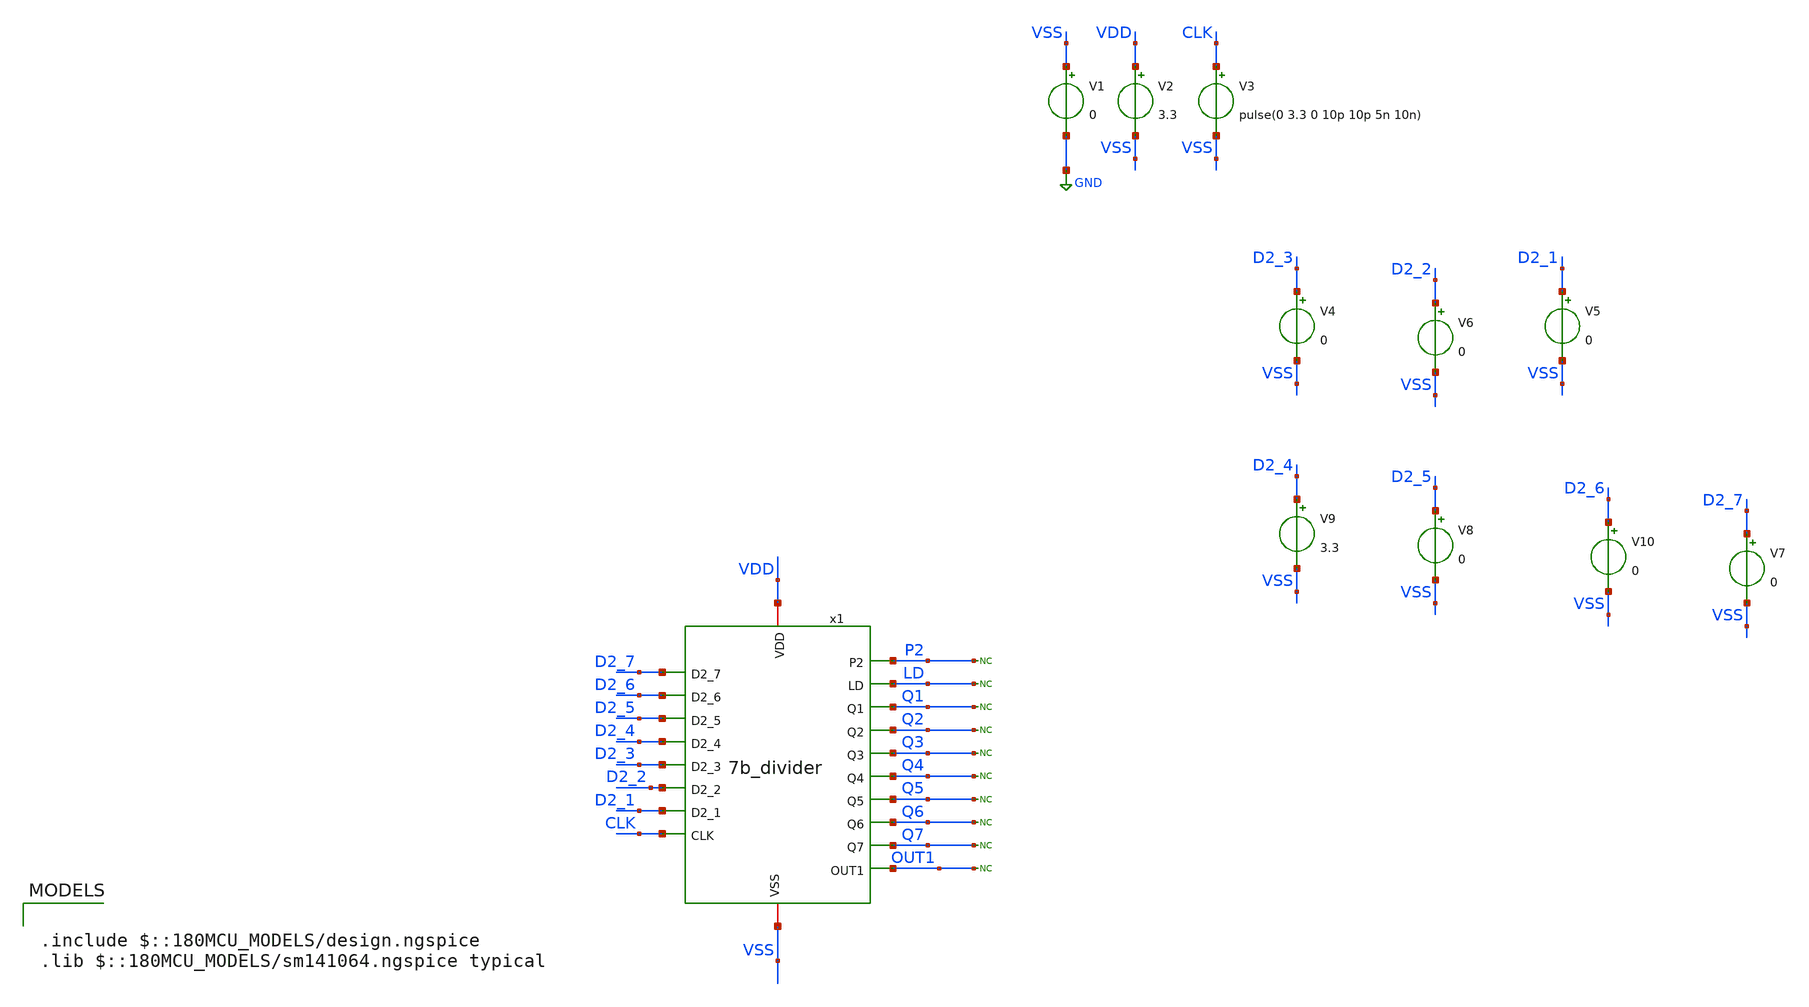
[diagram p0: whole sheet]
** sch_path: PLL-main/testbench/tran/xschem/7b_divider_tb.sch
**.subckt 7b_divider_tb
V1 VSS GND 0
V2 VDD VSS 3.3
V3 CLK VSS pulse(0 3.3 0 10p 10p 5n 10n)
V5 D2_1 VSS 0
V9 D2_4 VSS 3.3
V7 D2_7 VSS 0
V10 D2_6 VSS 0
V8 D2_5 VSS 0
V4 D2_3 VSS 0
V6 D2_2 VSS 0
x1 VDD LD D2_7 Q1 D2_6 Q2 D2_5 D2_4 Q3 Q4 D2_3 D2_2 Q5 D2_1 Q6 Q7 CLK VSS OUT1 P2 7b_divider
* noconn P2
* noconn LD
* noconn Q1
* noconn Q2
* noconn Q3
* noconn Q4
* noconn Q5
* noconn Q6
* noconn Q7
* noconn OUT1
**** begin user architecture code


*.option savecurrents
*.include pex_7b_divider_magic.spice
.control
save all

tran 100n 5u
set xbrushwidth=2
set xfontsize=3
plot v(CLK) v(Q3)+3.5 v(Q2)+7 v(Q1)+10.5 v(P2)+14 v(x1.P0)+17.5 v(OUT1)+21 v(LD)+24.5 v(Q4)+28
+ v(Q5)+31.5
plot v(Q1)
plot v(Q2)
plot v(Q3) v(Q2) v(Q1)
write 7b_divider_tb.raw
*write test_nfet_03v3.raw
.endc



.include $::180MCU_MODELS/design.ngspice
.lib $::180MCU_MODELS/sm141064.ngspice typical

**** end user architecture code
**.ends
.GLOBAL GND
.end
